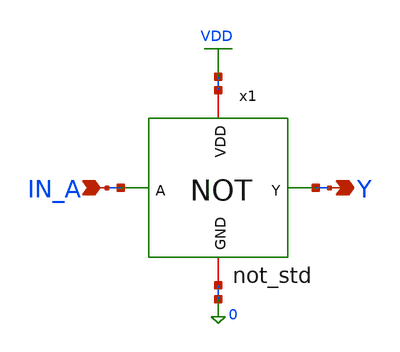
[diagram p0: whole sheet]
** sch_path: parity_ceker/testbench/tb_not.sch
**.subckt tb_not IN_A Y
*.ipin IN_A
*.opin Y
x1 VDD IN_A Y 0 not_std
**** begin user architecture code

.lib /foss/pdks/sky130A/libs.tech/ngspice/sky130.lib.spice tt

* --- 0. VOLTAGE SOURCES ---
V_SUPPLY VDD 0 1.8
* IN_A period is 40ns, IN_B period is 20ns to test all 4 states (00, 01, 10, 11)
V_A IN_A 0 pulse(0 1.8 1ns 100ps 100ps 19ns 40ns)
V_B IN_B 0 pulse(0 1.8 1ns 100ps 100ps 9ns 20ns)

* --- 1. SIMULATION COMMANDS ---
.tran 10p 100n
.dc V_A 0 1.8 0.01
.save all

.control
  run

  * --- 2. VISUAL THEME (WHITE BACKGROUND) ---
  set color0=white
  set color1=black
  set color2=red
  set color3=blue
  set color4=darkgreen
  set xbrushwidth=3

  * --- 3. TIMING & POWER ANALYSIS ---
  setplot tran1

  * Universal Delay: measures time between first input crossing and first output crossing
  meas tran t_delay trig v(in_a) val=0.9 cross=1 targ v(y) val=0.9 cross=1

  * Power Analysis
  meas tran avg_i avg i(V_SUPPLY)
  let p_dyn = avg_i * 1.8 * -1

  meas tran leak_i find i(V_SUPPLY) at=99n
  let p_stat = leak_i * 1.8 * -1

  let pdp = p_dyn * t_delay

  * --- 4. EXPORT CLEAN REPORT ---
  * Note: Avoid double quotes to prevent Xschem parsing errors
  echo === UNIVERSAL GATE REPORT === > report.txt
  echo Propagation Delay: >> report.txt
  print t_delay >> report.txt
  echo Dynamic Power: >> report.txt
  print p_dyn >> report.txt
  echo Static Power: >> report.txt
  print p_stat >> report.txt
  echo Power Delay Product: >> report.txt
  print pdp >> report.txt

  * --- 5. ADVANCED DATA PROCESSING & RAW EXPORT ---
  setplot tran1
  let inst_power = -i(V_SUPPLY) * 1.8
  let total_energy = integ(inst_power)

  * Export pristine raw simulation data for Gaw / GTKWave
  write universal_gate.raw

  * --- 6. EXPORT PLOTS (SVG) ---
  set hcopydevtype=svg

  * Save DC Sweeps
  setplot dc1
  hardcopy dc_vtc.svg v(y) vs v(in_a) title 'DC: VTC'
  hardcopy dc_gain.svg v(y) vs v(in_a) deriv(v(y)) xl 0 1.8 yl -5 1.8 title 'DC: VTC and Noise Margins'

  * Save Transient Plots (Separated cleanly)
  setplot tran1
  hardcopy tran_inputs.svg v(in_a) v(in_b) title 'Transient: Logic Inputs'
  hardcopy tran_output.svg v(y) title 'Transient: Logic Output'
  hardcopy tran_current.svg -i(V_SUPPLY) title 'Transient: Total Supply Current'
  hardcopy tran_energy.svg total_energy title 'Transient: Cumulative Energy'
  hardcopy tran_leakage.svg -i(V_SUPPLY) yl 0 10n title 'Transient: Static Leakage Zoom'

  * --- 7. SHOW PLOTS ON SCREEN ---
  * DC Plots
  setplot dc1
  plot v(y) vs v(in_a) title 'VTC'
  plot v(y) vs v(in_a) deriv(v(y)) xl 0 1.8 yl -5 1.8 title 'VTC and Noise Margins'

  * Transient Plots (Separated cleanly)
  setplot tran1
  plot v(in_a) v(in_b) title 'Logic Inputs (IN_A, IN_B)'
  plot v(y) title 'Logic Output (Y)'
  plot -i(V_SUPPLY) title 'Total Supply Current (Crowbar & Dynamic)'
  plot total_energy title 'Cumulative Energy Consumption'
  plot -i(V_SUPPLY) yl 0 10n title 'Static Leakage Current Zoom'
.endc

**** end user architecture code
**.ends

* expanding   symbol:  schematic/not_std.sym # of pins=4
** sym_path: parity_ceker/schematic/not_std.sym
** sch_path: parity_ceker/schematic/not_std.sch
.subckt not_std VDD A Y GND
*.ipin A
*.opin Y
*.iopin VDD
*.iopin GND
XM1 Y A VDD VDD sky130_fd_pr__pfet_01v8 L=0.15 W=2 nf=1 ad='int((1 + 1)/2) * 2 / 1 * 0.29' as='int((1 + 2)/2) * 2 / 1 * 0.29'
+ pd='2*int((1 + 1)/2) * (2 / 1 + 0.29)' ps='2*int((1 + 2)/2) * (2 / 1 + 0.29)' nrd='0.29 / 2 ' nrs='0.29 / 2 '
+ sa=0 sb=0 sd=0 mult=1 m=1
XM2 Y A GND GND sky130_fd_pr__nfet_01v8 L=0.15 W=1 nf=1 ad='int((1 + 1)/2) * 1 / 1 * 0.29' as='int((1 + 2)/2) * 1 / 1 * 0.29'
+ pd='2*int((1 + 1)/2) * (1 / 1 + 0.29)' ps='2*int((1 + 2)/2) * (1 / 1 + 0.29)' nrd='0.29 / 1 ' nrs='0.29 / 1 '
+ sa=0 sb=0 sd=0 mult=1 m=1
.ends

.GLOBAL VDD
.end
